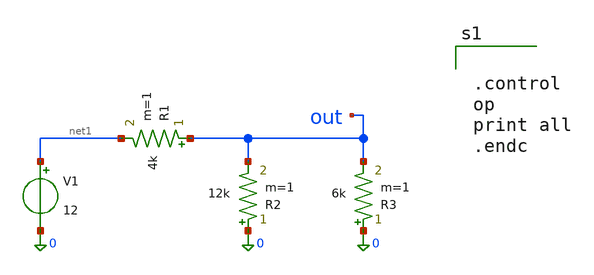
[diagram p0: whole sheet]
** sch_path: schem/d1.sch
**.subckt d1
V1 net1 0 12
R1 out net1 4k m=1
R2 0 out 12k m=1
R3 0 out 6k m=1
**** begin user architecture code


.control
op
print all
.endc


**** end user architecture code
**.ends
.end
